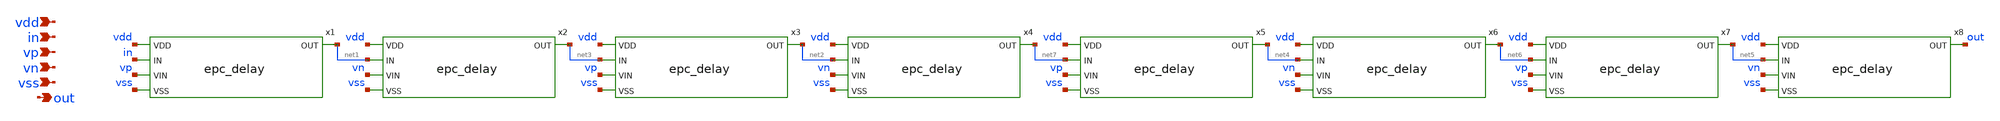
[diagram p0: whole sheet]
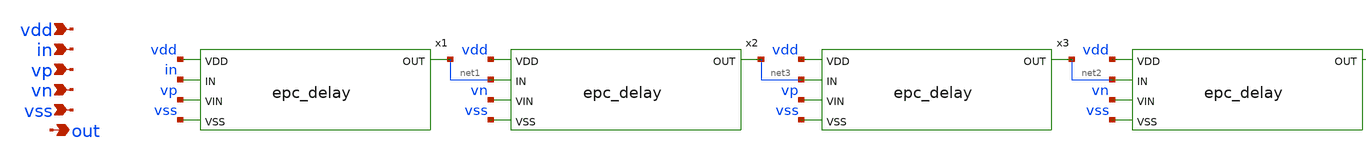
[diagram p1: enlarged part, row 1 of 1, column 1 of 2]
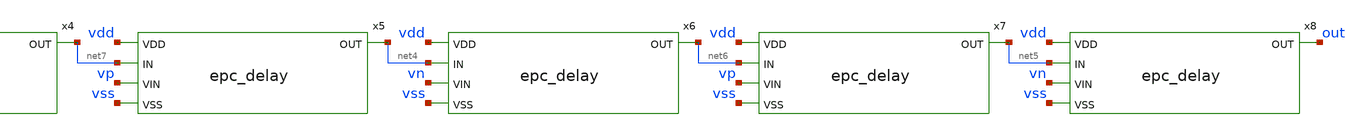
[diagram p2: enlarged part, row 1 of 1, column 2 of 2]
** sch_path: xschem/epc_delay_line.sch
**.subckt epc_delay_line vdd in vp vn vss out
*.ipin vdd
*.ipin in
*.ipin vp
*.ipin vn
*.ipin vss
*.opin out
x1 vdd in net1 vp vss epc_delay
x2 vdd net1 net3 vn vss epc_delay
x3 vdd net3 net2 vp vss epc_delay
x4 vdd net2 net7 vn vss epc_delay
x5 vdd net7 net4 vp vss epc_delay
x6 vdd net4 net6 vn vss epc_delay
x7 vdd net6 net5 vp vss epc_delay
x8 vdd net5 out vn vss epc_delay
**.ends

* expanding   symbol:  epc_delay.sym # of pins=5
** sym_path: epc_delay.sym
** sch_path: epc_delay.sch
.subckt epc_delay VDD IN OUT VIN VSS
*.ipin VDD
*.ipin VIN
*.ipin IN
*.ipin VSS
*.opin OUT
.param W_N=0.5 L_N=0.5 W_P=1.0 L_P=0.5
XM1 net2 VIN VDD VDD sky130_fd_pr__pfet_01v8_lvt L=L_P W=W_P nf=1 ad='int((nf+1)/2) * W/nf * 0.29' as='int((nf+2)/2) * W/nf * 0.29'
+ pd='2*int((nf+1)/2) * (W/nf + 0.29)' ps='2*int((nf+2)/2) * (W/nf + 0.29)' nrd='0.29 / W' nrs='0.29 / W'
+ sa=0 sb=0 sd=0 mult=1 m=1
XM2 OUT IN net2 VDD sky130_fd_pr__pfet_01v8_lvt L=L_P W=W_P nf=1 ad='int((nf+1)/2) * W/nf * 0.29' as='int((nf+2)/2) * W/nf * 0.29'
+ pd='2*int((nf+1)/2) * (W/nf + 0.29)' ps='2*int((nf+2)/2) * (W/nf + 0.29)' nrd='0.29 / W' nrs='0.29 / W'
+ sa=0 sb=0 sd=0 mult=1 m=1
XM3 OUT IN net1 VSS sky130_fd_pr__nfet_01v8_lvt L=L_N W=W_N nf=1 ad='int((nf+1)/2) * W/nf * 0.29' as='int((nf+2)/2) * W/nf * 0.29'
+ pd='2*int((nf+1)/2) * (W/nf + 0.29)' ps='2*int((nf+2)/2) * (W/nf + 0.29)' nrd='0.29 / W' nrs='0.29 / W'
+ sa=0 sb=0 sd=0 mult=1 m=1
XM4 net1 VIN VSS VSS sky130_fd_pr__nfet_01v8_lvt L=L_N W=W_N nf=1 ad='int((nf+1)/2) * W/nf * 0.29' as='int((nf+2)/2) * W/nf * 0.29'
+ pd='2*int((nf+1)/2) * (W/nf + 0.29)' ps='2*int((nf+2)/2) * (W/nf + 0.29)' nrd='0.29 / W' nrs='0.29 / W'
+ sa=0 sb=0 sd=0 mult=1 m=1
.ends

.end
